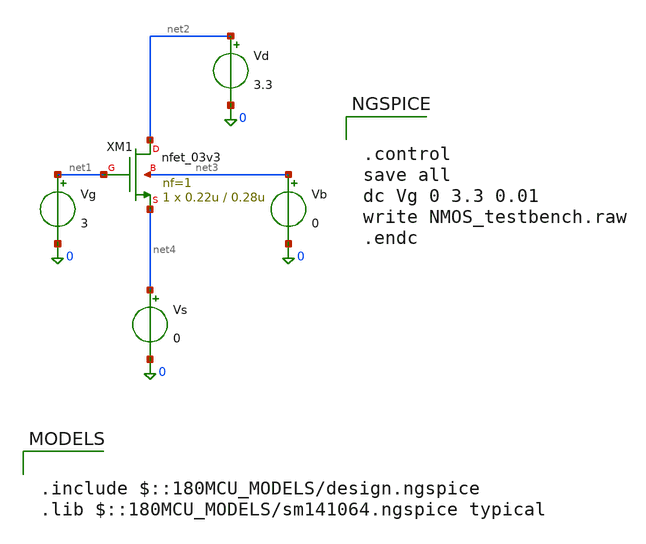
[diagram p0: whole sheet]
** sch_path: 3_Examples/FET_Characterization/NMOS_testbench.sch
**.subckt NMOS_testbench
XM1 net2 net1 net4 net3 nfet_03v3 L=0.28u W=0.22u nf=1 ad='int((nf+1)/2) * W/nf * 0.18u' as='int((nf+2)/2) * W/nf * 0.18u'
+ pd='2*int((nf+1)/2) * (W/nf + 0.18u)' ps='2*int((nf+2)/2) * (W/nf + 0.18u)' nrd='0.18u / W' nrs='0.18u / W'
+ sa=0 sb=0 sd=0 m=1 par=1
Vg net1 0 3
Vs net4 0 0
Vb net3 0 0
Vd net2 0 3.3
**** begin user architecture code

.include $::180MCU_MODELS/design.ngspice
.lib $::180MCU_MODELS/sm141064.ngspice typical



.control
save all
dc Vg 0 3.3 0.01
write NMOS_testbench.raw
.endc


**** end user architecture code
**.ends
.end
